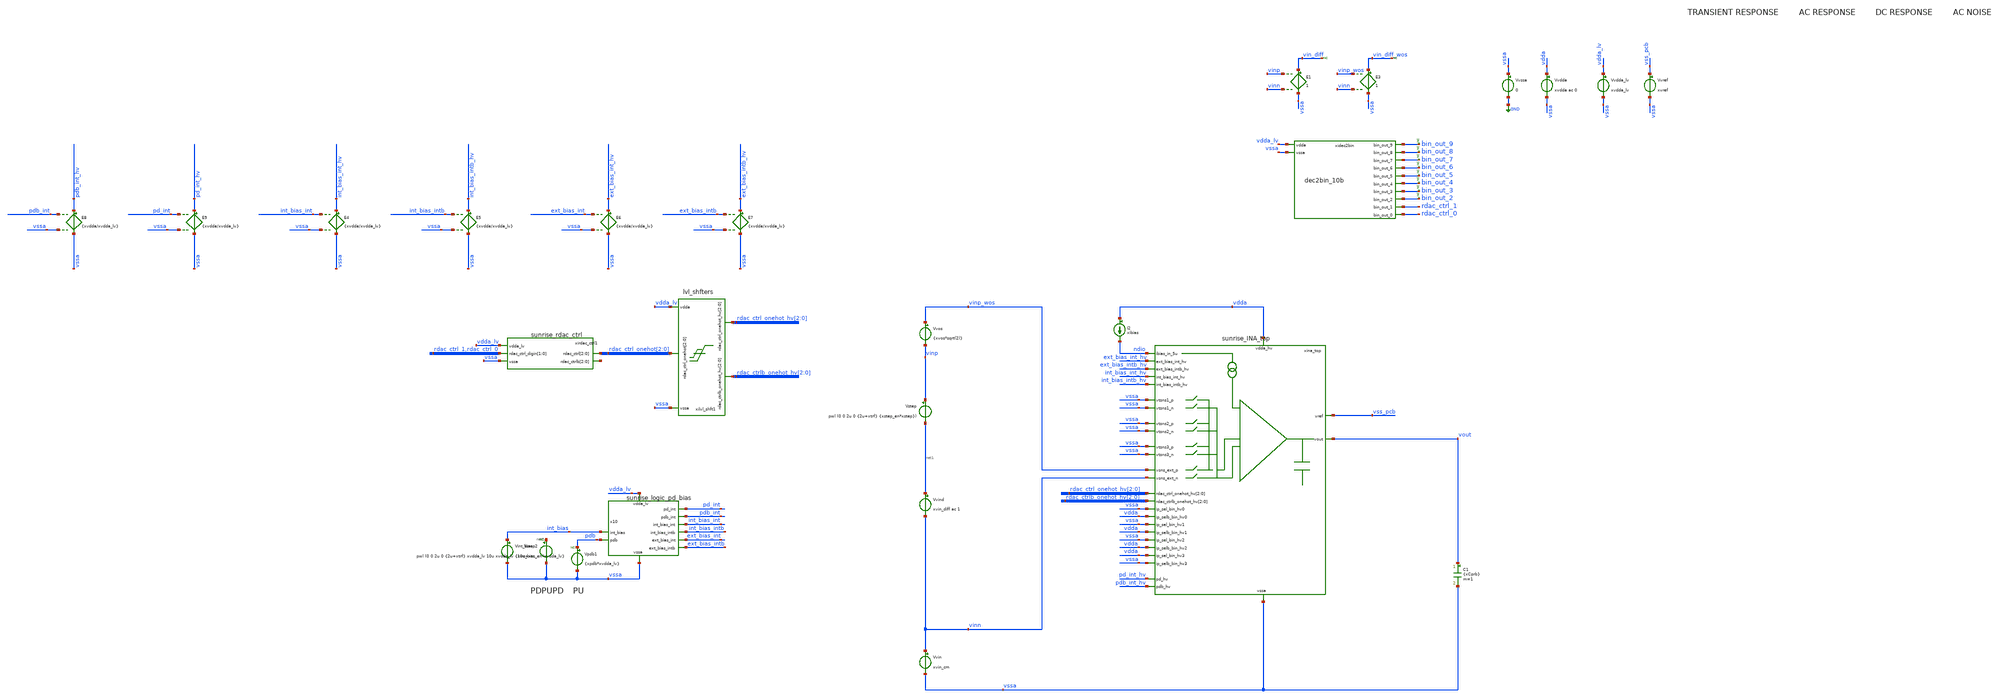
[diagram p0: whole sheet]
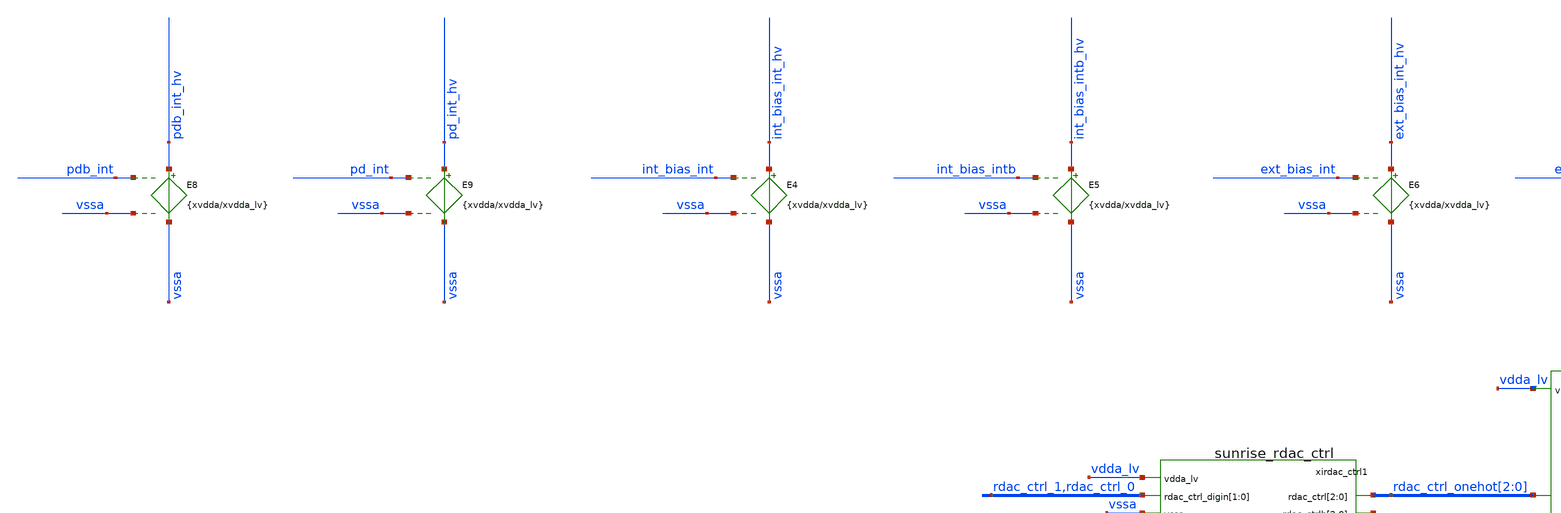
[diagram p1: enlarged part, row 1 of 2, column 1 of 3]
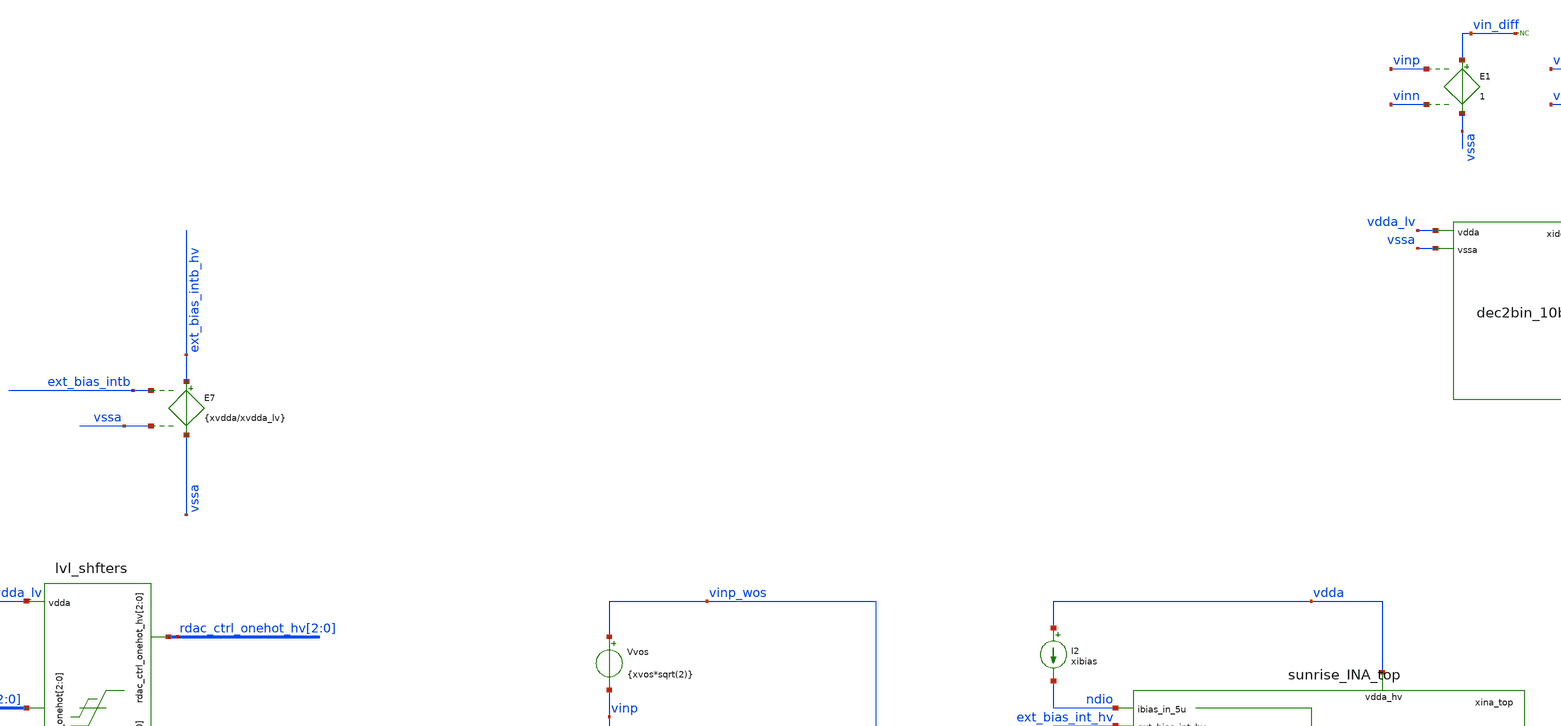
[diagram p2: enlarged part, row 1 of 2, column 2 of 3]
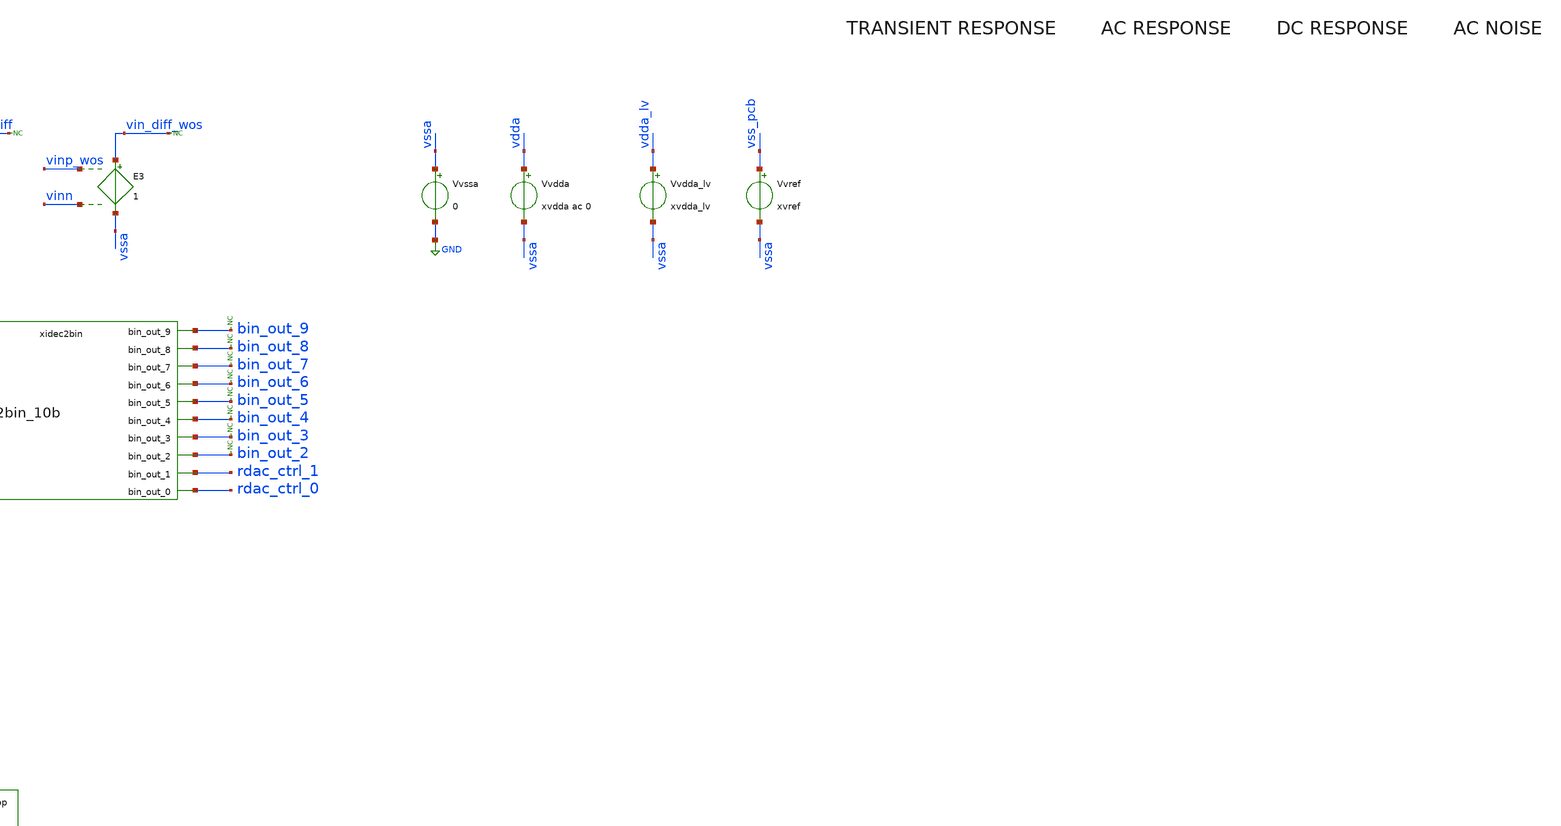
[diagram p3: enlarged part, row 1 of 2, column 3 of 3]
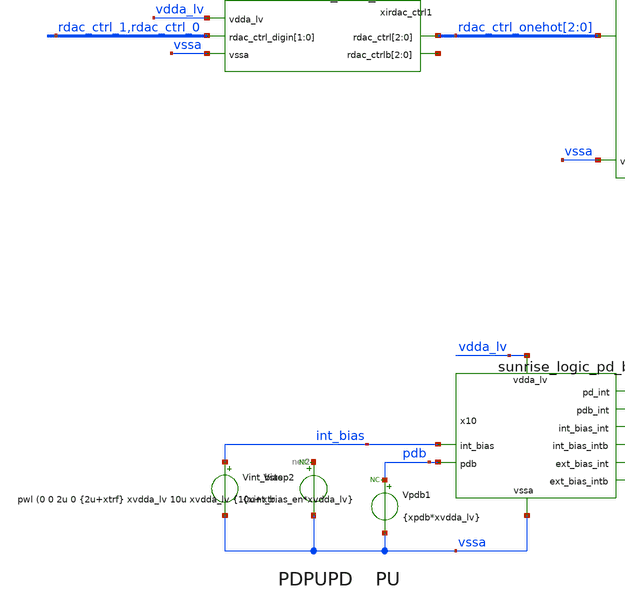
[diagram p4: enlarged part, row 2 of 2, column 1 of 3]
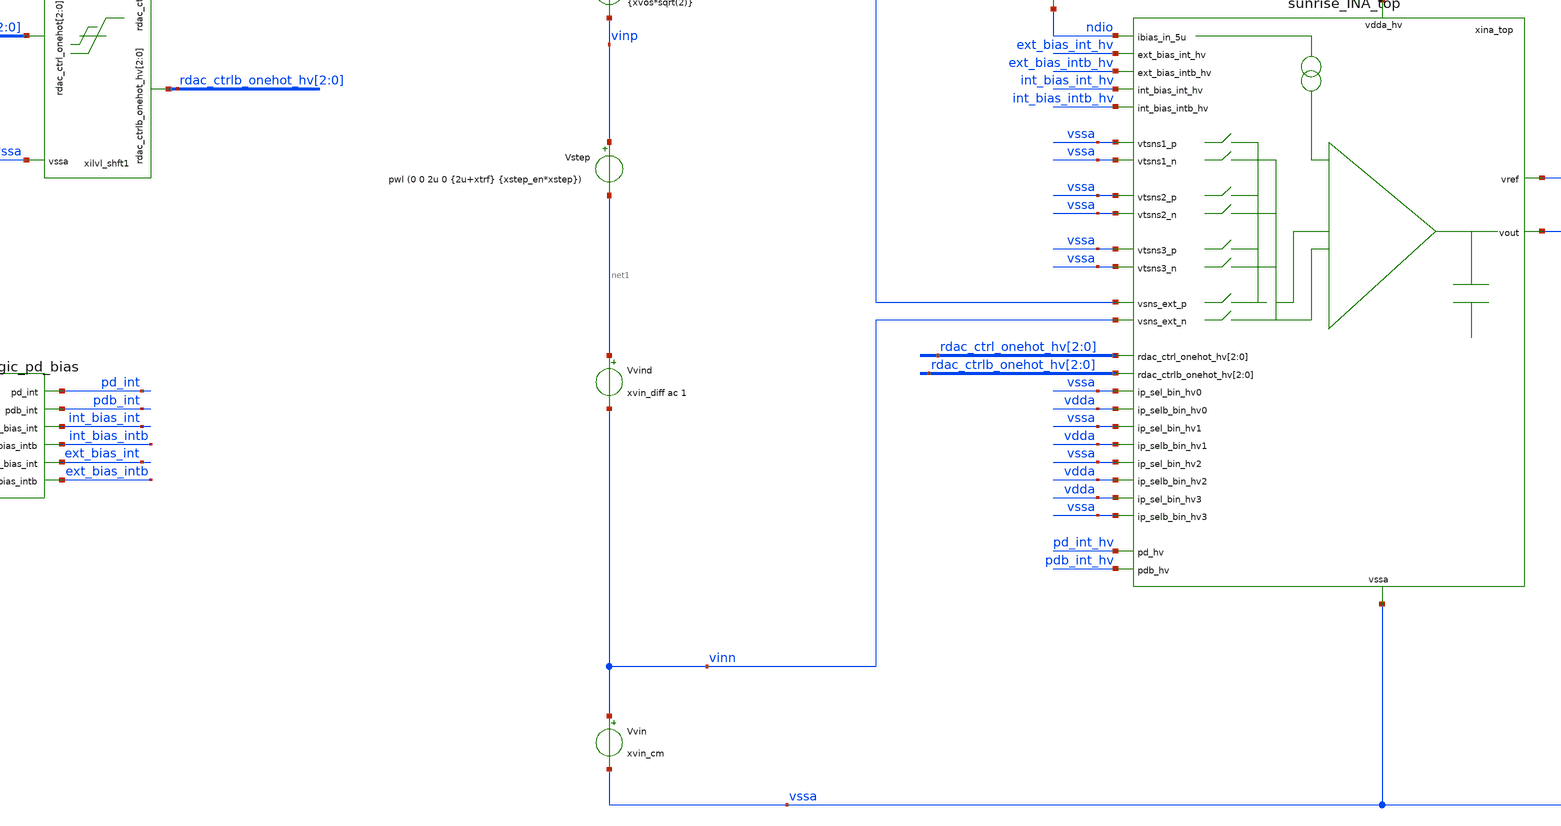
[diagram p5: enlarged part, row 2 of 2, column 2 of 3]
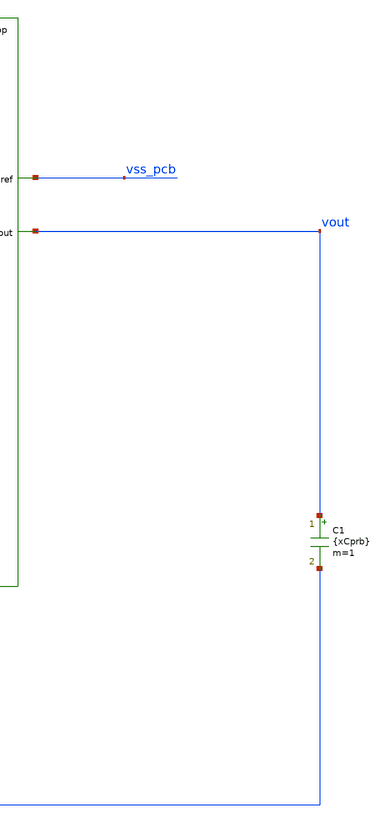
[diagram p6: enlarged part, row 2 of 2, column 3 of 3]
** sch_path: Design_Review_2/INA/Testbench_5_tb_sunrise_ina_top_OS_STB_BW_NOISE/tb_sunrise_ina_top_OS_STB_BW_NOISE.sch
**.subckt tb_sunrise_ina_top_OS_STB_BW_NOISE
Vvssa vssa GND 0
C1 vout vssa {xCprb} m=1
Vvin vinn vssa xvin_cm
Vvind net1 vinn xvin_diff ac 1
E1 vin_diff vssa vinp vinn 1
Vvref vss_pcb vssa xvref
* noconn vin_diff
Vvos vinp_wos vinp {xvos*sqrt(2)}
E3 vin_diff_wos vssa vinp_wos vinn 1
* noconn vin_diff_wos
Vvdda_lv vdda_lv vssa xvdda_lv
xidec2bin bin_out_9 bin_out_8 bin_out_7 bin_out_6 bin_out_5 bin_out_4 bin_out_3 bin_out_2
+ rdac_ctrl_1 rdac_ctrl_0 vdda_lv vssa dec2bin_10b dec_code=dec_code_var
* noconn bin_out_9
* noconn bin_out_8
* noconn bin_out_7
* noconn bin_out_6
* noconn bin_out_5
* noconn bin_out_4
* noconn bin_out_3
* noconn bin_out_2
Vvdda vdda vssa xvdda ac 0
Vstep vinp net1 pwl (0 0 2u 0 {2u+xtrf} {xstep_en*xstep})
Vint_bias int_bias vssa {xint_bias_en*xvdda_lv}
Vstep2 net2 vssa pwl (0 0 2u 0 {2u+xtrf} xvdda_lv 10u xvdda_lv {10u+xtrf} 0)
Vpdb1 pdb vssa {xpdb*xvdda_lv}
* noconn pdb
* noconn #net2
E4 int_bias_int_hv vssa int_bias_int vssa {xvdda/xvdda_lv}
E5 int_bias_intb_hv vssa int_bias_intb vssa {xvdda/xvdda_lv}
E6 ext_bias_int_hv vssa ext_bias_int vssa {xvdda/xvdda_lv}
E7 ext_bias_intb_hv vssa ext_bias_intb vssa {xvdda/xvdda_lv}
E8 pdb_int_hv vssa pdb_int vssa {xvdda/xvdda_lv}
E9 pd_int_hv vssa pd_int vssa {xvdda/xvdda_lv}
xina_top vssa vssa vdda vssa vssa ndio ext_bias_int_hv vssa ext_bias_intb_hv int_bias_int_hv vss_pcb
+ int_bias_intb_hv vssa vinp_wos vout vinn rdac_ctrl_onehot_hv[2] rdac_ctrl_onehot_hv[1] rdac_ctrl_onehot_hv[0]
+ rdac_ctrlb_onehot_hv[2] rdac_ctrlb_onehot_hv[1] rdac_ctrlb_onehot_hv[0] vssa vdda pd_int_hv pdb_int_hv vssa vssa vdda vssa
+ vdda vdda vssa sunrise_INA_top
I2 vdda ndio xibias
xilvl_shft1 rdac_ctrl_onehot[2] rdac_ctrl_onehot[1] rdac_ctrl_onehot[0] rdac_ctrlb_onehot_hv[2]
+ rdac_ctrlb_onehot_hv[1] rdac_ctrlb_onehot_hv[0] vssa rdac_ctrl_onehot_hv[2] rdac_ctrl_onehot_hv[1] rdac_ctrl_onehot_hv[0]
+ vdda_lv lvl_shfters
xirdac_ctrl1 rdac_ctrl_1 rdac_ctrl_0 rdac_ctrl_onehot[2] rdac_ctrl_onehot[1] rdac_ctrl_onehot[0]
+ vdda_lv vssa net3[2] net3[1] net3[0] sunrise_rdac_ctrl
x10 vdda_lv vssa int_bias_intb int_bias int_bias_int pdb ext_bias_intb ext_bias_int pdb_int pd_int
+ sunrise_logic_pd_bias
**** begin user architecture code

** opencircuitdesign pdks install
.lib /home/slice/pdk/iHP/IHP-Open-PDK/ihp-sg13g2/libs.tech/ngspice/models/cornerMOSlv.lib mos_tt
.lib /home/slice/pdk/iHP/IHP-Open-PDK/ihp-sg13g2/libs.tech/ngspice/models/cornerMOShv.lib mos_tt
.lib /home/slice/pdk/iHP/IHP-Open-PDK/ihp-sg13g2/libs.tech/ngspice/models/cornerRES.lib res_typ
* SG13G2 STD CELLS
*.include /home/slice/pdk/iHP/IHP-Open-PDK/ihp-sg13g2/libs.ref/sg13g2_stdcell/spice/sg13g2_stdcell.spice
* SG13CMOS5L STD CELLS
.include /home/slice/pdk/iHP/IHP-Open-PDK/ihp-sg13cmos5l/libs.ref/sg13cmos5l_stdcell/spice/sg13cmos5l_stdcell.spice

*.lib /home/slice/pdk/iHP/IHP-Open-PDK/ihp-sg13g2/libs.tech/ngspice/models/cornerMOShv.lib mos_ss
*.lib /home/slice/pdk/iHP/IHP-Open-PDK/ihp-sg13g2/libs.tech/ngspice/models/cornerRES.lib res_wcs


** PARAMETERS **

* global parameters
.param xvdda = 3.3
.csparam xvdda_hv_var = 'xvdda'
.param xvdda_lv = 1.5
.csparam xvdda_lv_var = 'xvdda_lv'
.param cor_id = 0
.csparam cor_id_var = 'cor_id'
.param xtsim = 20u
.csparam xtsim_var = 'xtsim'
.param xibias = 5u
.param xCfilt = 5p
.param xCprb = 20p
.param xtstep = 100n
.csparam xtstep_var = 'xtstep'
.param xdc_step = 10m
.csparam xdc_step_var = 'xdc_step'
.param xvos = 0m
.param xint_bias_en = 0
* active lo => 0 = pd
.param xpdb = 1
.param xnoise_stg1 = 1
.param xnoise_stg1_ia = 1
.param xnoise_stg1_nia = 1
.param xnoise_stg1_rg = 1
.param xnoise_stg2 = 1
.param xstep = 10m
.param xtrf = 20p
.param xstep_en = 1

* input swing parameters
* Below assumes you want a full input swing
* this is the margin between the supplies which vout can swing to
.param xvmargin = 50m
* max vout
.param xvin_diff_for_vout_max =  (xvdda-(2*xvmargin))/xAv_ina
.csparam xvin_diff_for_vout_max_var = 'xvin_diff_for_vout_max'
* min vout
.param xvin_diff_for_vout_min =  (xvmargin/xAv_ina)
.csparam xvin_diff_for_vout_min_var = 'xvin_diff_for_vout_min'

* set xvin_diff according to desired vout (max or min)
*.param xvin_diff = xvin_diff_for_vout_max

* note on vin_cm: vin_cm_min = max(1V,xAv_ia*vd_max).
* The 1V is due to the NMOS dp and means you cant sense < 1V.
* If you set vcm = xAv_ia*vd_max (assuming this is > 1V),
* you will get a full signal swing at the input (=xvdda/xAv_ina).
* If vcm gets larger, the NIA starts to saturate so dvin needs to be
* be < xvdda/xAv_ina. vin_cm_max simply equals xvdda.
.param xvin_cm = (xAv_ia*((xvdda-(2*xvmargin))/xAv_ina))+xvmargin

* Below assumes you want to pick specific values
*.param xvin_cm = 1.65
.csparam xvin_cm_var = 'xvin_cm'
.param xvin_diff = 10m

* set to the below to measure offset
*.param xvin_diff = 0

* ota model parameters
.param xAv0_dB = 70
.param xAv0 = 10^(xAv0_dB/20)
.param xgmdp = 1m
.param xGBW = 1Meg

* stg1 parameters
* Av = 1 => xRg = 50G, Av = 5 => xRg = 50k, Av = 11 => xRg = 20k, Av = 21 => xRg = 10k
.param xRg= 50k
.param dec_code_var = 1
.csparam xdec_code_var = 'dec_code_var'
* below is to ensure gain error due to xRsw < 1%
*.param xRsw = xRg/100
* below is to manually enter a value for xRsw
.param xRsw = 100
.param xRfb_stg1 = 100k
.param xAv_stg1 = 1+((2*xRfb_stg1)/xRg)
.csparam xAv_stg1_var = 'xAv_stg1'
.param xbeta_stg1 = 1/xAv_stg1
.param lg_stg1 = xAv0*xbeta_stg1
.csparam lg_stg1_var = 'lg_stg1'
.param xAv_ia = xRfb_stg1/xRg

* stg2 parameters
.param xvref = 3.3/2
*.param xvref = 50m
.param xRin_stg2 = 10k
.param xRfb_stg2 = 10k
.param xAv_stg2 = xRfb_stg2/xRin_stg2
.csparam xAv_stg2_var = 'xAv_stg2'
.param xbeta_stg2 = xRin_stg2/(xRin_stg2+xRfb_stg2)
.param lg_stg2 = xAv0*xbeta_stg2
.csparam lg_stg2_var = 'lg_stg2'

* total ina gain parameter
.param xAv_ina = xAv_stg1*xAv_stg2
.csparam xAv_ina_var = 'xAv_ina'

.temp 27

* vlogA instantiations
.model OTA_vcvs OTA_vcvs
.model ideal_sw ideal_sw
.model dec2bin_10b dec2bin_10b

.include tb_sunrise_ina_top_OS_STB_BW_NOISE.save

* below line needs to be included if running ac noise analysys
.save all


*.option savecurrents

*.save onoise* inoise* frequency
.save i(v.xstb.Vi) v(xstb.x) v(av)
.save v(vinp) v(vinn) v(vinp_wos) v(vin_diff) v(vin_diff_wos) v(vfb_ni) v(vfb_i) v(vih) v(vil) v(vip_stg2) v(vin_stg2) v(vin_stg2_diff) v(vout)
.save v(vdda) v(vdda_lv) v(vssa) v(vss_pcb) v(ibias1) v(ibias2) v(ibias3) v(vfb_ni2) v(vfb_i2) v(rdac_ctrl_1) v(rdac_ctrl_0)
.save v(xirdac.xirdac_ctrl.rdac_ctrl_int[0]) v(xirdac.xirdac_ctrl.rdac_ctrlb_int[0]) v(xirdac.xirdac_ctrl.rdac_ctrl_int[1]) v(xirdac.xirdac_ctrl.rdac_ctrlb_int[1]) v(xirdac.rdac_ctrl_onehot[2]) v(xirdac.rdac_ctrl_onehot[1]) v(xirdac.rdac_ctrl_onehot[0]) v(xirdac.rdac_ctrl_onehot_hv[2]) v(xirdac.rdac_ctrl_onehot_hv[1]) v(xirdac.rdac_ctrl_onehot_hv[0]) v(xirdac.rdac_ctrlb_onehot_hv[2]) v(xirdac.rdac_ctrlb_onehot_hv[1]) v(xirdac.rdac_ctrlb_onehot_hv[0])



.control

pre_osdi OTA_vcvs.osdi
pre_osdi ideal_sw.osdi
pre_osdi dec2bin_10b.osdi

 * commercial temperature range
 *set xTj = ( 0 10 20 30 40 50 60 70 )
 * industrial temperature range
 *set xTj = ( -40 -30 -20 -10 0 10 20 30 40 50 60 70 85 )
 * military temperature range
 *set xTj = ( -55 -40 -30 -20 -10 0 10 20 30 40 50 60 70 80 90 100 110 125 )
 * automotive temperature range
 *set xTj = ( -40 -30 -20 -10 0 10 20 30 40 50 60 70 80 90 100 110 120 130 140 150 )
 set xTj = ( 27 )

  foreach xTj_var $xTj

  let Tj_meas = $xTj_var

  echo temperature is "$&Tj_meas"

  *echo "$&Tj_meas" >> Temp_measures.txt

  set temp = $xTj_var
  echo $temp

** 1. DCOP ANALYSIS **

  op
  remzerovec
  set filetype=binary
  ** first write deletes existing file
  write tb_sunrise_ina_dcop.raw

** 2. TRAN ANALYSIS **

  *remzerovec *** always put remzerovec after the analysis!!!
  *set appendwrite
  tran $&xtstep_var $&xtsim_var
  remzerovec
  write tb_sunrise_ina_tran.raw
 *unset appendwrite

** 3. TRAN MEASURES **

  echo --
  *meas tran iddahv_ave AVG i(Vvdda) from=100n to=$&xtsim_var
  *meas tran vout_ave AVG v(vout) from=100n to=$&xtsim_var
  meas tran iddahv_ave AVG i(Vvdda) from=100n to=1.9u
  meas tran vout_ave AVG v(vout) from=100n to=1.9u
  let iddahv_ave_uA = iddahv_ave*(-1e6)

  * 3.0 Global parameters:
  echo cor_id = "$&cor_id_var"
  echo "$&cor_id_var" > iddahv_uA.txt
  echo "$&cor_id_var" > vout_v.txt
  echo --
  echo temp = "$temp"
  echo "$temp" >> iddahv_uA.txt
  echo "$temp" >> vout_v.txt
  echo --
  echo vdda_hv = "$&xvdda_hv_var"
  echo "$&xvdda_hv_var" >> iddahv_uA.txt
  echo "$&xvdda_hv_var" >> vout_v.txt
  echo --
  echo vdda_lv = "$&xvdda_lv_var"
  echo "$&xvdda_lv_var" >> iddahv_uA.txt
  echo "$&xvdda_lv_var" >> vout_v.txt
  echo --
  echo --
  echo  iddahv_A = "$&iddahv_ave"
  print iddahv_ave_uA
  echo "$&iddahv_ave_uA" >> iddahv_uA.txt
  echo "$&vout_ave" >> vout_v.txt
  echo --

** 4. AC ANALYSIS **

  ac dec 10 1 10G

  remzerovec
  write tb_sunrise_ina_ac.raw


** 5. AC MEASURES **

  * 5.0 Global parameters:
  echo cor_id = "$&cor_id_var"
  echo "$&cor_id_var" > ac_measures.txt
  echo --
  echo temp = "$temp"
  echo "$temp" >> ac_measures.txt
  echo --
  echo vdda_hv = "$&xvdda_hv_var"
  echo "$&xvdda_hv_var" >> ac_measures.txt
  echo --
  echo vdda_lv = "$&xvdda_lv_var"
  echo "$&xvdda_lv_var" >> ac_measures.txt
  echo --
  let n45_rads = -45*(pi/180)
  meas AC BW WHEN vp(vout)=n45_rads CROSS=1
  echo "$&BW" >> ac_measures.txt
  echo --

** 6. AC NOISE ANALYSIS **

  * 5.0 Global parameters:
  echo cor_id = "$&cor_id_var"
  echo "$&cor_id_var" > noise_ipr_1k.txt
  echo "$&cor_id_var" > noise_int.txt
  echo --
  echo temp = "$temp"
  echo "$temp" >> noise_ipr_1k.txt
  echo "$temp" >> noise_int.txt
  echo --
  echo vdda_hv = "$&xvdda_hv_var"
  echo "$&xvdda_hv_var" >> noise_ipr_1k.txt
  echo "$&xvdda_hv_var" >> noise_int.txt
  echo --
  echo vdda_lv = "$&xvdda_lv_var"
  echo "$&xvdda_lv_var" >> noise_ipr_1k.txt
  echo "$&xvdda_lv_var" >> noise_int.txt
  echo --

  let xfmax = 1G

  noise v(vout) Vvdda dec 10 10 $&xfmax 1

  setplot noise1
  set filetype=binary
  remzerovec
  write tb_sunrise_ina_noise_density.raw
  let vnoise_op_int = sqrt(integ(onoise_spectrum*onoise_spectrum))

  * generice code to measure noise densities at specified frequencies

  let freq_density1 = 1k
  let freq_density2 = 10k
  let freq_density3 = 100k

  let nn = 0
  while frequency[nn] < $&freq_density1
  let nn = nn + 1
  end
  * define vectors of frequncies and values just above and below
  * selected frequeny
  let fnn = frequency[nn]
  let nn1 = nn + 1
  let fnn1 = frequency[nn1]
  let snn = onoise_spectrum[nn]
  let snn1 = onoise_spectrum[nn1]
  *print vector values
  echo --
  echo nn = "$&nn"  freq_density1 = "$&fnn"  noise_density1 = "$&snn"
  echo nn1 = "$&nn1"  freq_density1+ = "$&fnn1"  noise_density1+ = "$&snn1"
  *linear interpolation for exact frequency
  let newsnn = snn1 + (snn - snn1)/(fnn - fnn1)*($&freq_density1 - fnn1)
  let newsnn_ipr = newsnn/$&xAv_ina_var
  echo  freq_density1 = "$&freq_density1"  noise_density1_interp_opr = "$&newsnn"
  echo Av_ina = "$&xAv_ina_var"
  echo  freq_density1 = "$&freq_density1"  noise_density1_interp_ipr = "$&newsnn_ipr"
  echo "$&newsnn_ipr" >> noise_ipr_1k.txt
  echo --

  let nn = 0
  while frequency[nn] < $&freq_density2
  let nn = nn + 1
  end
  * define vectors of frequncies and values just above and below
  * selected frequeny
  let fnn = frequency[nn]
  let nn1 = nn + 1
  let fnn1 = frequency[nn1]
  let snn = onoise_spectrum[nn]
  let snn1 = onoise_spectrum[nn1]
  *print vector values
  echo --
  echo nn = "$&nn"  freq_density2 = "$&fnn"  noise_density2 = "$&snn"
  echo nn1 = "$&nn1"  freq_density2+ = "$&fnn1"  noise_density2+ = "$&snn1"
  *linear interpolation for exact frequency
  let newsnn = snn1 + (snn - snn1)/(fnn - fnn1)*($&freq_density2 - fnn1)
  let newsnn_ipr = newsnn/$&xAv_ina_var
  echo  freq_density2 = "$&freq_density2"  noise_density2_interp_opr = "$&newsnn"
  echo Av_ina = "$&xAv_ina_var"
  echo  freq_density2 = "$&freq_density2"  noise_density2_interp_ipr = "$&newsnn_ipr"
  *echo "$&newsnn_ipr" >> noise_ipr_10k.txt
  echo --

  let nn = 0
  while frequency[nn] < $&freq_density3
  let nn = nn + 1
  end
  * define vectors of frequncies and values just above and below
  * selected frequeny
  let fnn = frequency[nn]
  let nn1 = nn + 1
  let fnn1 = frequency[nn1]
  let snn = onoise_spectrum[nn]
  let snn1 = onoise_spectrum[nn1]
  *print vector values
  echo --
  echo nn = "$&nn"  freq_density3 = "$&fnn"  noise_density3 = "$&snn"
  echo nn1 = "$&nn1"  freq_density3+ = "$&fnn1"  noise_density3+ = "$&snn1"
  *linear interpolation for exact frequency
  let newsnn = snn1 + (snn - snn1)/(fnn - fnn1)*($&freq_density3 - fnn1)
  let newsnn_ipr = newsnn/$&xAv_ina_var
  echo  freq_density3 = "$&freq_density3"  noise_density3_interp_opr = "$&newsnn"
  echo Av_ina = "$&xAv_ina_var"
  echo  freq_density3 = "$&freq_density3"  noise_density3_interp_ipr = "$&newsnn_ipr"
  *echo "$&newsnn_ipr" >> noise_ipr_100k.txt
  echo --

  setplot noise2
  print v(onoise_total)
  echo "$&v(onoise_total)" >> noise_int.txt
  set filetype=ascii
  remzerovec
  write tb_sunrise_ina_integrated_noise.raw

  end

  setplot
*quit 0
.endc




**** end user architecture code
**.ends
.GLOBAL GND
.end
